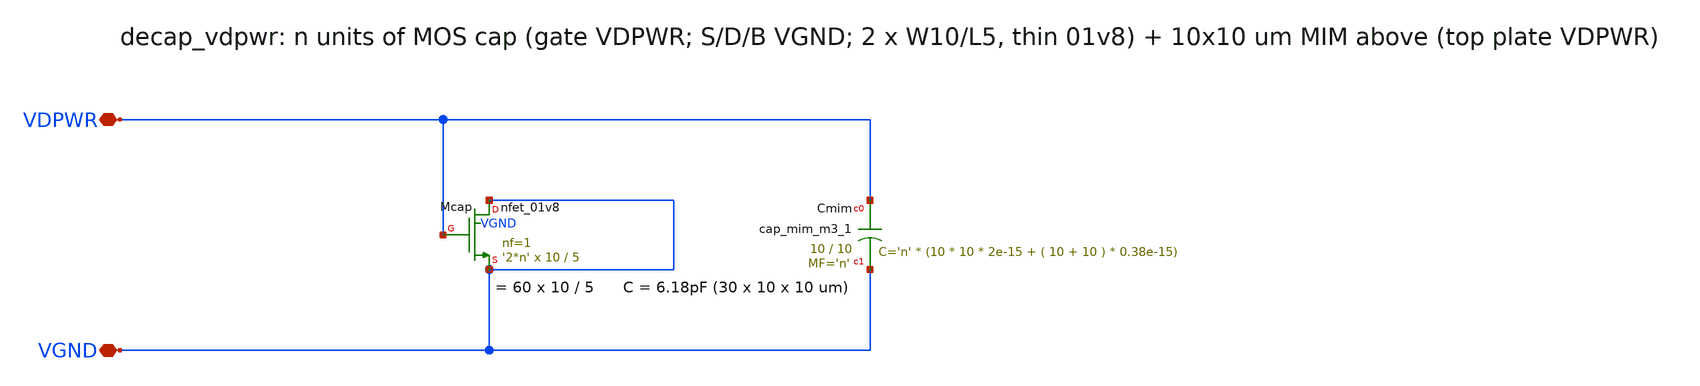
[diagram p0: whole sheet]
** sch_path: xschem/decap_vdpwr.sch
**.subckt decap_vdpwr VDPWR VGND
*.iopin VDPWR
*.iopin VGND
XMcap VGND VDPWR VGND VGND sky130_fd_pr__nfet_01v8 L=5 W=10 nf=1 ad='int((nf+1)/2) * W/nf * 0.29' as='int((nf+2)/2) * W/nf * 0.29'
+ pd='2*int((nf+1)/2) * (W/nf + 0.29)' ps='2*int((nf+2)/2) * (W/nf + 0.29)' nrd='0.29 / W' nrs='0.29 / W'
+ sa=0 sb=0 sd=0 mult='2*n' m='2*n'
XCmim VDPWR VGND sky130_fd_pr__cap_mim_m3_1 W=10 L=10 MF='n' m='n'
**.ends
.end
